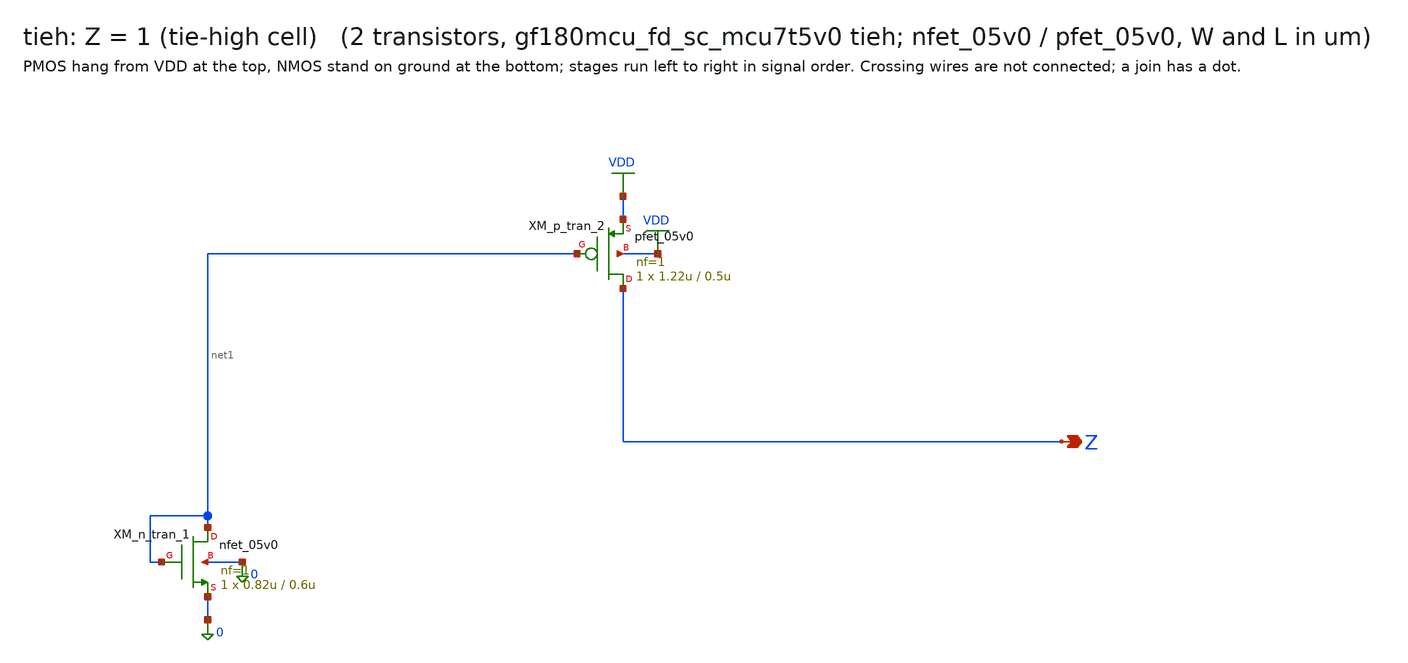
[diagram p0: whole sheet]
** sch_path: xschem/cells_tx/tieh.sch
**.subckt tieh Z
*.opin Z
XM_n_tran_1 net1 net1 0 0 nfet_05v0 L=0.6u W=0.82u nf=1 ad=4.1e-13 as=4.1e-13 pd=2.64e-06
+ ps=2.64e-06 nrd=0 nrs=0 sa=0 sb=0 sd=0 m=1
XM_p_tran_2 Z net1 VDD VDD pfet_05v0 L=0.5u W=1.22u nf=1 ad=6.1e-13 as=6.1e-13 pd=3.44e-06
+ ps=3.44e-06 nrd=0 nrs=0 sa=0 sb=0 sd=0 m=1
**.ends
.GLOBAL VDD
.end
